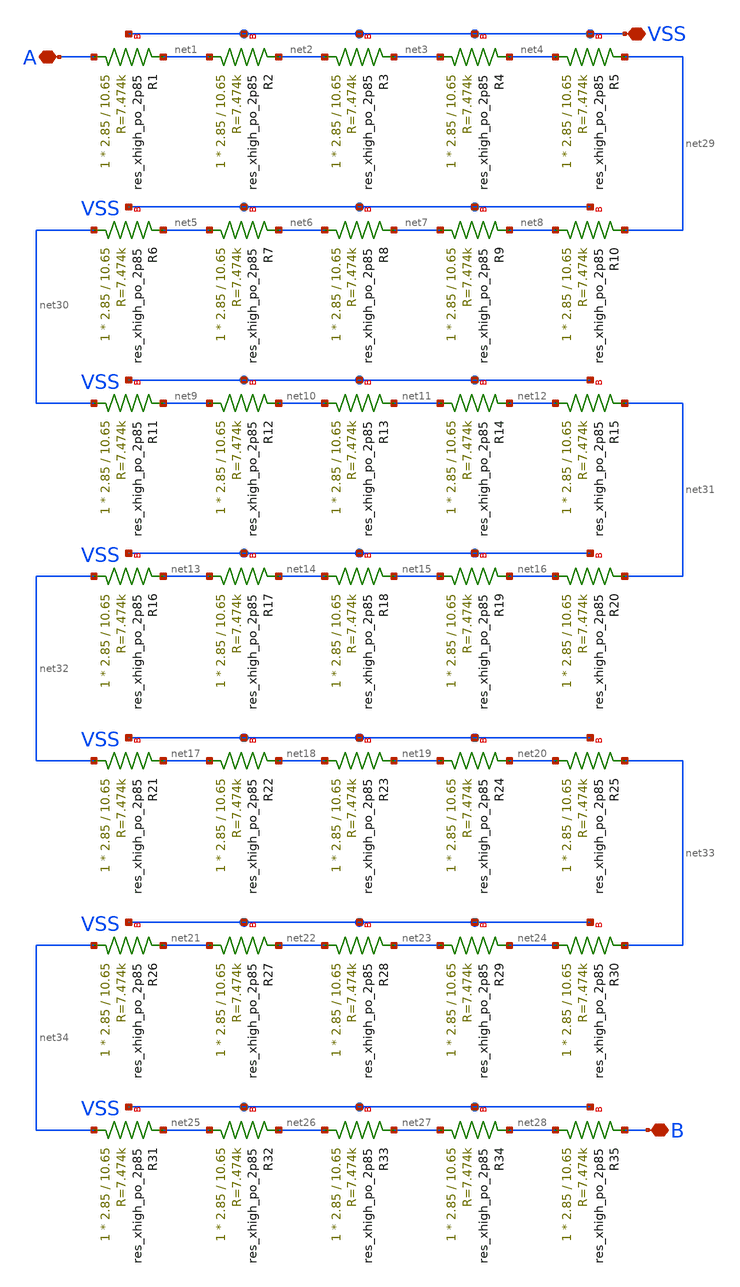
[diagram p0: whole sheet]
** sch_path: integrasi/integrasi/serpentine_res/topology3/untitled.sch
**.subckt untitled A B VSS
*.iopin A
*.iopin B
*.iopin VSS
XR1 A net1 VSS sky130_fd_pr__res_xhigh_po_2p85 L=10.65 mult=1 m=1
XR2 net1 net2 VSS sky130_fd_pr__res_xhigh_po_2p85 L=10.65 mult=1 m=1
XR3 net2 net3 VSS sky130_fd_pr__res_xhigh_po_2p85 L=10.65 mult=1 m=1
XR4 net3 net4 VSS sky130_fd_pr__res_xhigh_po_2p85 L=10.65 mult=1 m=1
XR5 net4 net29 VSS sky130_fd_pr__res_xhigh_po_2p85 L=10.65 mult=1 m=1
XR6 net30 net5 VSS sky130_fd_pr__res_xhigh_po_2p85 L=10.65 mult=1 m=1
XR7 net5 net6 VSS sky130_fd_pr__res_xhigh_po_2p85 L=10.65 mult=1 m=1
XR8 net6 net7 VSS sky130_fd_pr__res_xhigh_po_2p85 L=10.65 mult=1 m=1
XR9 net7 net8 VSS sky130_fd_pr__res_xhigh_po_2p85 L=10.65 mult=1 m=1
XR10 net8 net29 VSS sky130_fd_pr__res_xhigh_po_2p85 L=10.65 mult=1 m=1
XR11 net30 net9 VSS sky130_fd_pr__res_xhigh_po_2p85 L=10.65 mult=1 m=1
XR12 net9 net10 VSS sky130_fd_pr__res_xhigh_po_2p85 L=10.65 mult=1 m=1
XR13 net10 net11 VSS sky130_fd_pr__res_xhigh_po_2p85 L=10.65 mult=1 m=1
XR14 net11 net12 VSS sky130_fd_pr__res_xhigh_po_2p85 L=10.65 mult=1 m=1
XR15 net12 net31 VSS sky130_fd_pr__res_xhigh_po_2p85 L=10.65 mult=1 m=1
XR16 net32 net13 VSS sky130_fd_pr__res_xhigh_po_2p85 L=10.65 mult=1 m=1
XR17 net13 net14 VSS sky130_fd_pr__res_xhigh_po_2p85 L=10.65 mult=1 m=1
XR18 net14 net15 VSS sky130_fd_pr__res_xhigh_po_2p85 L=10.65 mult=1 m=1
XR19 net15 net16 VSS sky130_fd_pr__res_xhigh_po_2p85 L=10.65 mult=1 m=1
XR20 net16 net31 VSS sky130_fd_pr__res_xhigh_po_2p85 L=10.65 mult=1 m=1
XR21 net32 net17 VSS sky130_fd_pr__res_xhigh_po_2p85 L=10.65 mult=1 m=1
XR22 net17 net18 VSS sky130_fd_pr__res_xhigh_po_2p85 L=10.65 mult=1 m=1
XR23 net18 net19 VSS sky130_fd_pr__res_xhigh_po_2p85 L=10.65 mult=1 m=1
XR24 net19 net20 VSS sky130_fd_pr__res_xhigh_po_2p85 L=10.65 mult=1 m=1
XR25 net20 net33 VSS sky130_fd_pr__res_xhigh_po_2p85 L=10.65 mult=1 m=1
XR26 net34 net21 VSS sky130_fd_pr__res_xhigh_po_2p85 L=10.65 mult=1 m=1
XR27 net21 net22 VSS sky130_fd_pr__res_xhigh_po_2p85 L=10.65 mult=1 m=1
XR28 net22 net23 VSS sky130_fd_pr__res_xhigh_po_2p85 L=10.65 mult=1 m=1
XR29 net23 net24 VSS sky130_fd_pr__res_xhigh_po_2p85 L=10.65 mult=1 m=1
XR30 net24 net33 VSS sky130_fd_pr__res_xhigh_po_2p85 L=10.65 mult=1 m=1
XR31 net34 net25 VSS sky130_fd_pr__res_xhigh_po_2p85 L=10.65 mult=1 m=1
XR32 net25 net26 VSS sky130_fd_pr__res_xhigh_po_2p85 L=10.65 mult=1 m=1
XR33 net26 net27 VSS sky130_fd_pr__res_xhigh_po_2p85 L=10.65 mult=1 m=1
XR34 net27 net28 VSS sky130_fd_pr__res_xhigh_po_2p85 L=10.65 mult=1 m=1
XR35 net28 B VSS sky130_fd_pr__res_xhigh_po_2p85 L=10.65 mult=1 m=1
**.ends
.end
